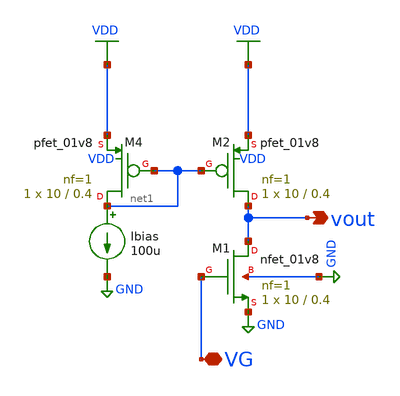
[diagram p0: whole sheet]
** sch_path: SelfStudy/Analog/Tony Chan/SpiceSim/cs.sch
**.subckt cs vout VG
*.opin vout
*.iopin VG
XM1 vout VG GND GND sky130_fd_pr__nfet_01v8 L=0.4 W=10 nf=1 ad='int((1 + 1)/2) * 10 / 1 * 0.29' as='int((1 + 2)/2) * 10 / 1 * 0.29'
+ pd='2*int((1 + 1)/2) * (10 / 1 + 0.29)' ps='2*int((1 + 2)/2) * (10 / 1 + 0.29)' nrd='0.29 / 10 ' nrs='0.29 / 10 '
+ sa=0 sb=0 sd=0 mult=1 m=1
Ibias net1 GND 100u
XM2 vout net1 VDD VDD sky130_fd_pr__pfet_01v8 L=0.4 W=10 nf=1 ad='int((1 + 1)/2) * 10 / 1 * 0.29' as='int((1 + 2)/2) * 10 / 1 * 0.29'
+ pd='2*int((1 + 1)/2) * (10 / 1 + 0.29)' ps='2*int((1 + 2)/2) * (10 / 1 + 0.29)' nrd='0.29 / 10 ' nrs='0.29 / 10 '
+ sa=0 sb=0 sd=0 mult=1 m=1
XM4 net1 net1 VDD VDD sky130_fd_pr__pfet_01v8 L=0.4 W=10 nf=1 ad='int((1 + 1)/2) * 10 / 1 * 0.29' as='int((1 + 2)/2) * 10 / 1 * 0.29'
+ pd='2*int((1 + 1)/2) * (10 / 1 + 0.29)' ps='2*int((1 + 2)/2) * (10 / 1 + 0.29)' nrd='0.29 / 10 ' nrs='0.29 / 10 '
+ sa=0 sb=0 sd=0 mult=1 m=1
**** begin user architecture code

.lib /usr/local/share/pdk/sky130A/libs.tech/ngspice/sky130.lib.spice tt

vsup VDD 0 1.8

vin vg dc=0 ac=1

.tran 10u 10m
.end

.control
run
plot v(VG) vs v(vout)
.endc


**** end user architecture code
**.ends
.GLOBAL GND
.GLOBAL VDD
.end
